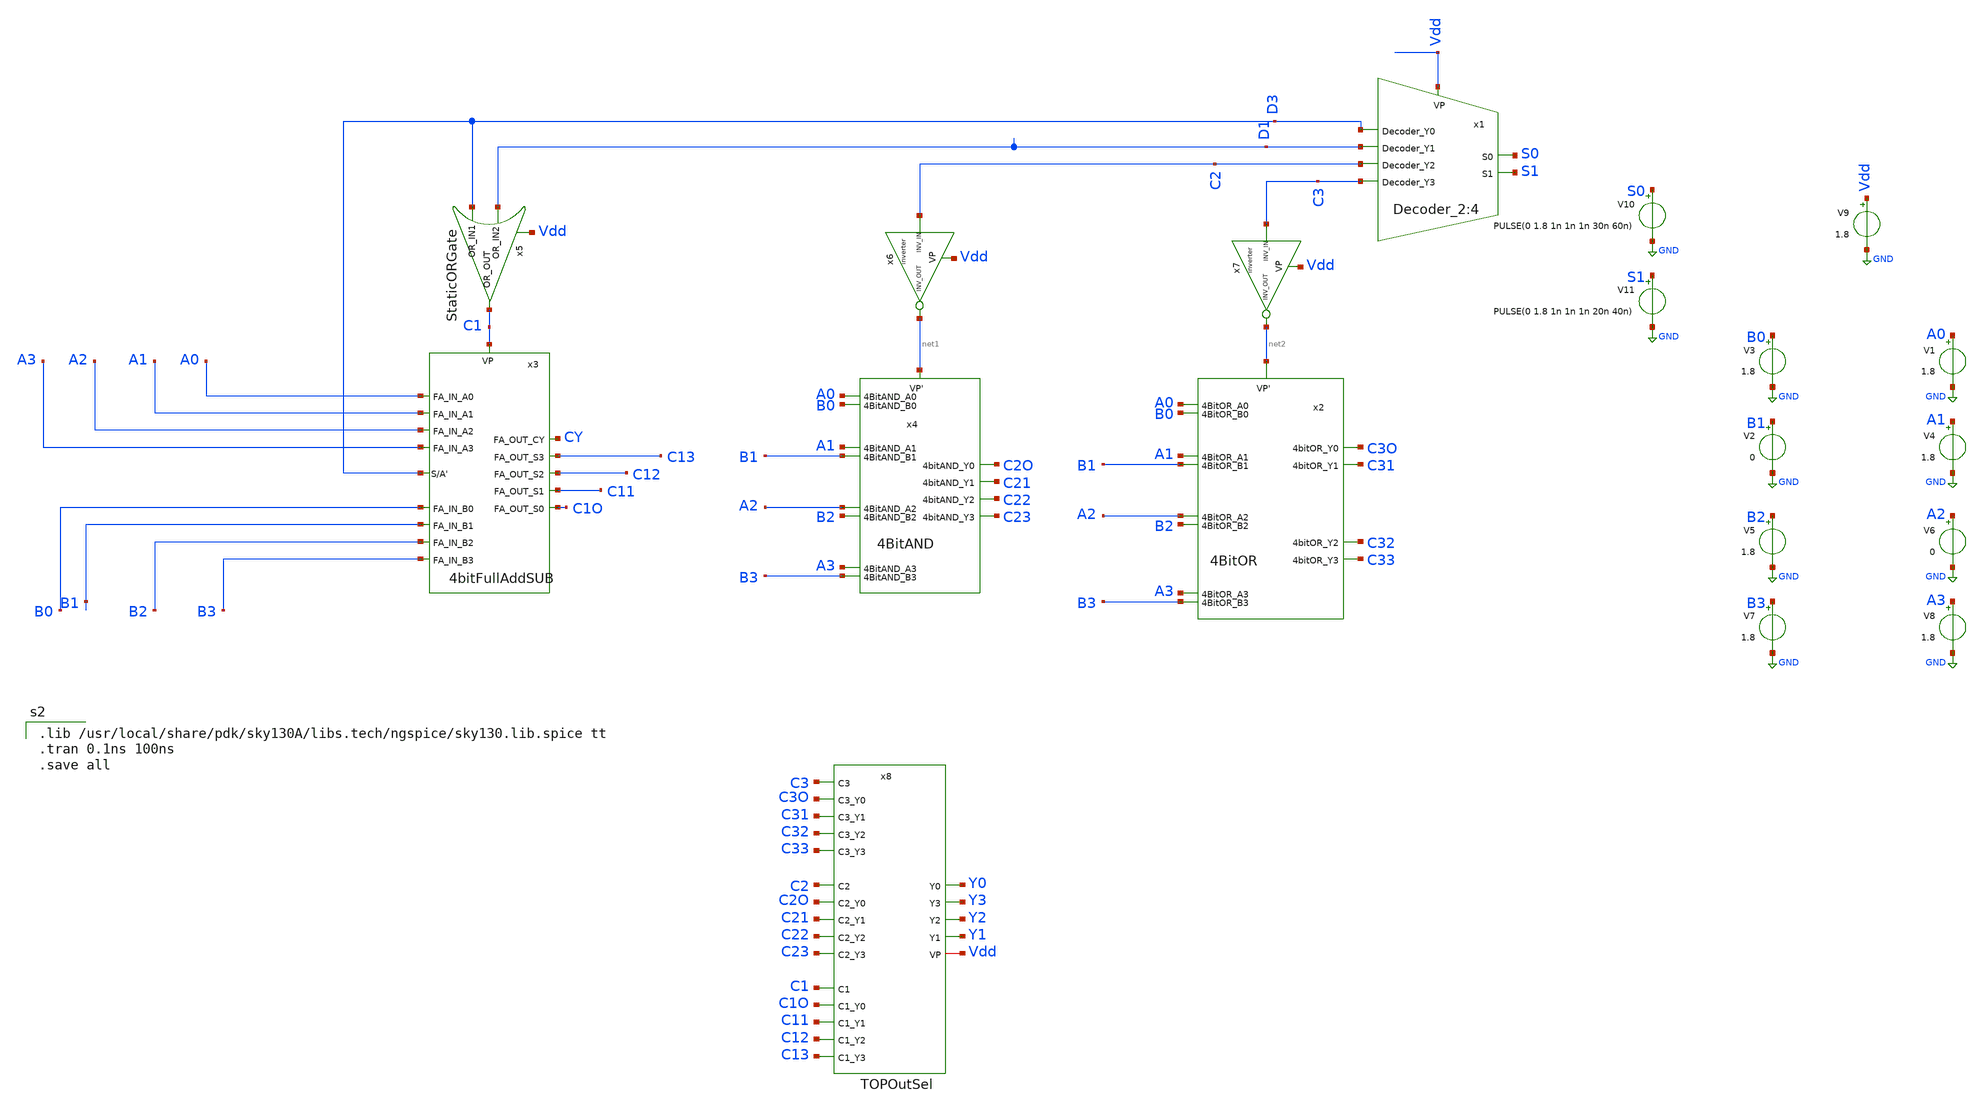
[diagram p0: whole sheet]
** sch_path: AllSymbols&Sch/AdderSubtractor/TryReuse.sch
**.subckt TryReuse
V3 B0 GND 1.8
V9 Vdd GND 1.8
V1 A0 GND 1.8
V2 B1 GND 0
V4 A1 GND 1.8
V5 B2 GND 1.8
V7 B3 GND 1.8
V8 A3 GND 1.8
V10 S0 GND PULSE(0 1.8 1n 1n 1n 30n 60n)
V11 S1 GND PULSE(0 1.8 1n 1n 1n 20n 40n)
V6 A2 GND 0
x3 A1 B1 B2 B3 A3 A2 B0 A0 C1 CY C13 C12 C11 C1O D3 4bitFullAddSUB
x2 A0 C3O B0 A1 C31 B1 A2 C32 B2 A3 C33 B3 net2 4BitOR
x4 A0 C2O B0 A1 C21 B1 A2 C22 B2 A3 C23 B3 net1 4BitAND
x1 S0 S1 D3 Vdd D1 C2 C3 Decoder_2:4
x5 D1 D3 C1 Vdd StaticORGate
x6 Vdd net1 C2 inverter
x7 Vdd net2 C3 inverter
x8 C3 C33 C31 C3O C32 C22 C23 C2O C21 Y0 Y3 Y2 Y1 C12 C13 C11 C1O C1 Vdd C2 TOPOutSel
**** begin user architecture code

.lib /usr/local/share/pdk/sky130A/libs.tech/ngspice/sky130.lib.spice tt
.tran 0.1ns 100ns
.save all





**** end user architecture code
**.ends
.GLOBAL GND
.end
